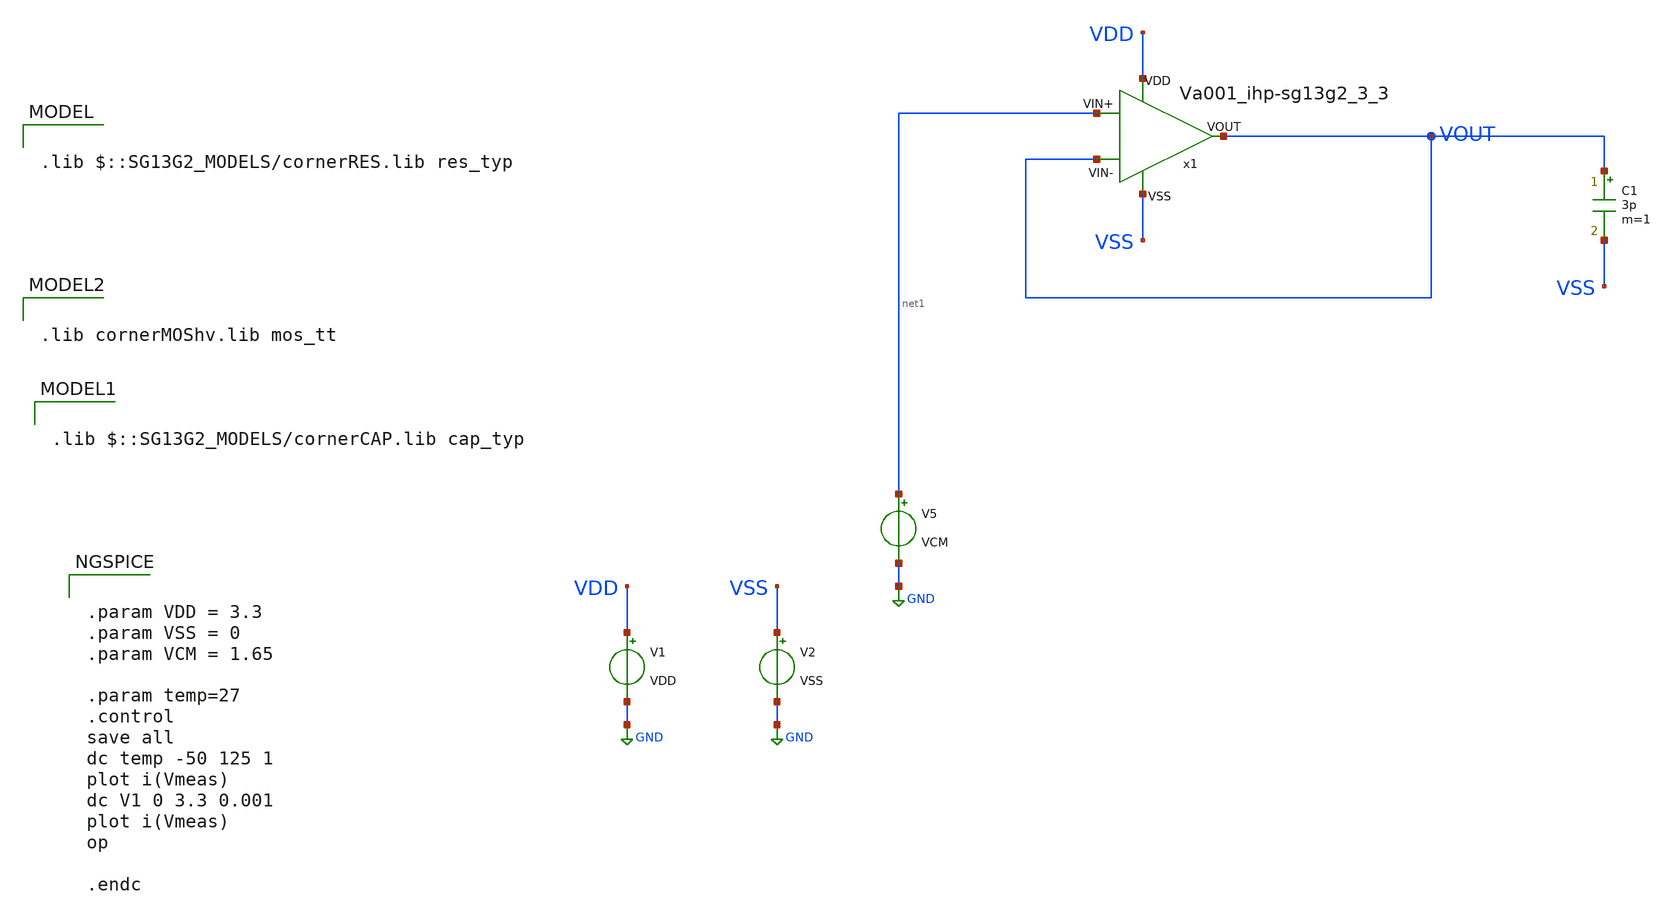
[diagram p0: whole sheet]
** sch_path: Learning/single_ended_amplifiers/Design_and_Analysis_of_Two-Stage_CMOS_Operational_Amplifier_for_Fluorescence_Signal_Processing_ihp130_3_3V/amplifier_design/single_tb.sch
**.subckt single_tb
x1 VDD VSS VOUT net1 VOUT Va001_ihp-sg13g2_3_3
V1 VDD GND VDD
V2 VSS GND VSS
V5 net1 GND VCM
C1 VOUT VSS 3p m=1
**** begin user architecture code

.lib $::SG13G2_MODELS/cornerRES.lib res_typ


.lib cornerMOShv.lib mos_tt


.lib $::SG13G2_MODELS/cornerCAP.lib cap_typ

**** end user architecture code
**.ends

* expanding   symbol:  ihp-sg13g2/Amplifiers/Va001_ihp-sg13g2_3_3.sym # of pins=5
** sym_path: LIB/ihp-sg13g2/Amplifiers/Va001_ihp-sg13g2_3_3.sym
** sch_path: LIB/ihp-sg13g2/Amplifiers/Va001_ihp-sg13g2_3_3.sch
.subckt Va001_ihp-sg13g2_3_3 VDD VSS VIN- VIN+ VOUT
*.iopin VDD
*.iopin VSS
*.iopin VIN-
*.iopin VIN+
*.iopin VOUT
XM2 VB1 VB1 VDD VDD sg13_hv_pmos w=1.5u l=2u ng=2 m=2 mm_ok=1
XM1 VB2 VB1 VDD VDD sg13_hv_pmos w=1.5u l=2u ng=2 m=2 mm_ok=1
XM3 net3 VB2 VB1 VSS sg13_hv_nmos w=1.0u l=2u ng=2 m=2 mm_ok=1
XM4 net1 VB2 VB2 VSS sg13_hv_nmos w=1.0u l=2u ng=2 m=2 mm_ok=1
XM5 net2 net1 net3 VSS sg13_hv_nmos w=2u l=2u ng=2 m=8 mm_ok=1
XM6 VSS net1 net1 VSS sg13_hv_nmos w=2u l=2u ng=2 m=2 mm_ok=1
XR1 net2 VSS sub! rhigh w=0.5e-6 l=5.9e-6 m=1 b=0 mm_ok=1
XM7 net4 VB1 VDD VDD sg13_hv_pmos w=1.5u l=2u ng=2 m=8 mm_ok=1
XM9 net6 VIN+ net4 net4 sg13_hv_pmos w=8u l=0.6 ng=4 m=4 mm_ok=1
XM8 net5 VIN- net4 net4 sg13_hv_pmos w=8u l=0.6 ng=4 m=4 mm_ok=1
XM10 VSS net5 net5 VSS sg13_hv_nmos w=2u l=2u ng=2 m=2 mm_ok=1
XM11 VSS net5 net6 VSS sg13_hv_nmos w=2u l=2u ng=2 m=2 mm_ok=1
XM12 VOUT VB1 VDD VDD sg13_hv_pmos w=1.5u l=2u ng=2 m=16 mm_ok=1
XM13 VSS net6 VOUT VSS sg13_hv_nmos w=2u l=0.8 ng=2 m=4 mm_ok=1
XM14 net6 VB2 net7 VSS sg13_hv_nmos w=2u l=2u ng=1 m=2 mm_ok=1
XC1 VOUT net7 cap_cmim w=8.0e-6 l=8.0e-6 m=1 mm_ok=1
.ends

.GLOBAL GND
**** begin user architecture code


.param VDD = 3.3
.param VSS = 0
.param VCM = 1.65

.param temp=27
.control
save all
dc temp -50 125 1
plot i(Vmeas)
dc V1 0 3.3 0.001
plot i(Vmeas)
op

.endc


**** end user architecture code
.end
